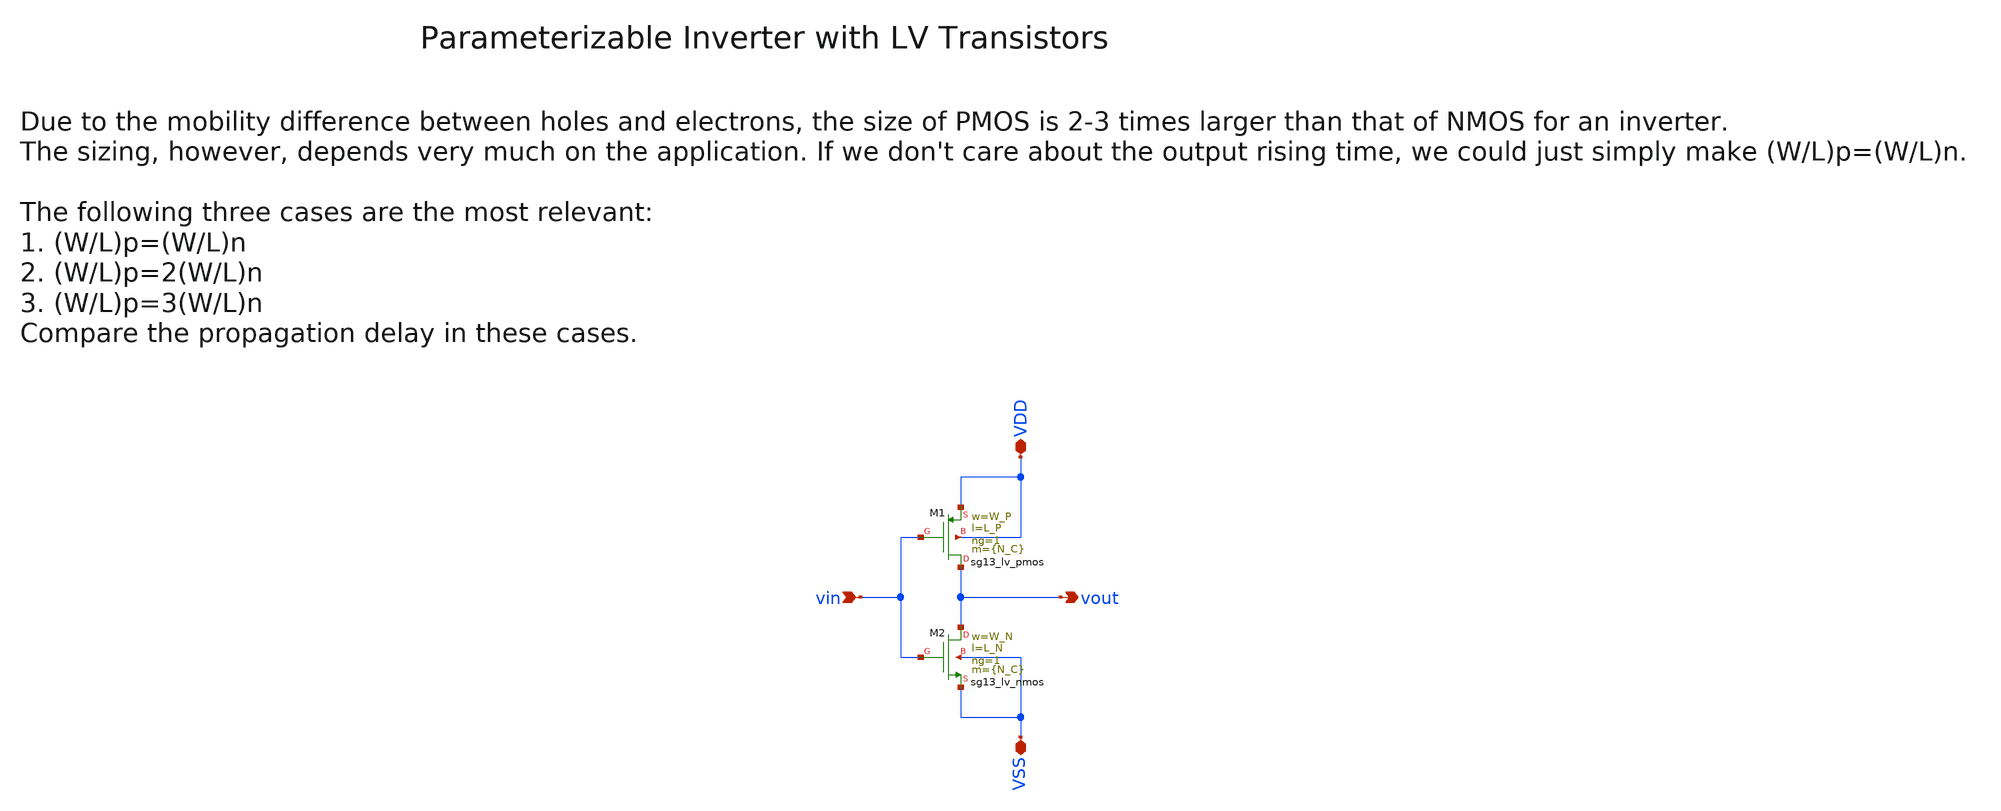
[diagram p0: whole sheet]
** sch_path: xschem/inverter/inverter_lv.sch
**.subckt inverter_lv vin VDD VSS vout
*.ipin vin
*.iopin VDD
*.iopin VSS
*.opin vout
XM1 vout vin VDD VDD sg13_lv_pmos w=W_P l=L_P ng=1 m={N_C} mm_ok=1
XM2 vout vin VSS VSS sg13_lv_nmos w=W_N l=L_N ng=1 m={N_C} mm_ok=1
**.ends
.end
